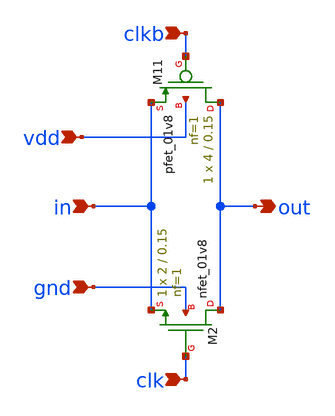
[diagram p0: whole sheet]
** sch_path: pll/dividers_lib/divider/xschem/TG.sch
**.subckt TG vdd in gnd clkb clk out
*.ipin vdd
*.ipin in
*.ipin gnd
*.ipin clkb
*.ipin clk
*.opin out
XM11 out clkb in vdd sky130_fd_pr__pfet_01v8 L=0.15 W=4 nf=1 ad='int((nf+1)/2) * W/nf * 0.29' as='int((nf+2)/2) * W/nf * 0.29'
+ pd='2*int((nf+1)/2) * (W/nf + 0.29)' ps='2*int((nf+2)/2) * (W/nf + 0.29)' nrd='0.29 / W' nrs='0.29 / W'
+ sa=0 sb=0 sd=0 mult=1 m=1
XM2 out clk in gnd sky130_fd_pr__nfet_01v8 L=0.15 W=2 nf=1 ad='int((1 + 1)/2) * 2 / 1 * 0.29' as='int((1 + 2)/2) * 2 / 1 * 0.29'
+ pd='2*int((1 + 1)/2) * (2 / 1 + 0.29)' ps='2*int((1 + 2)/2) * (2 / 1 + 0.29)' nrd='0.29 / 2 ' nrs='0.29 / 2 '
+ sa=0 sb=0 sd=0 mult=1 m=1
**.ends
.end
